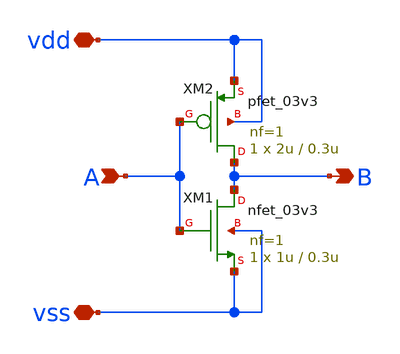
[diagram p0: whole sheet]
** sch_path: General/ADC/switching/inv4switch.sch
**.subckt inv4switch A B vdd vss
*.ipin A
*.opin B
*.iopin vdd
*.iopin vss
XM1 B A vss vss nfet_03v3 L=0.3u W=1u nf=1 ad='int((nf+1)/2) * W/nf * 0.18u' as='int((nf+2)/2) * W/nf * 0.18u'
+ pd='2*int((nf+1)/2) * (W/nf + 0.18u)' ps='2*int((nf+2)/2) * (W/nf + 0.18u)' nrd='0.18u / W' nrs='0.18u / W'
+ sa=0 sb=0 sd=0 m=1
XM2 B A vdd vdd pfet_03v3 L=0.3u W=2u nf=1 ad='int((nf+1)/2) * W/nf * 0.18u' as='int((nf+2)/2) * W/nf * 0.18u'
+ pd='2*int((nf+1)/2) * (W/nf + 0.18u)' ps='2*int((nf+2)/2) * (W/nf + 0.18u)' nrd='0.18u / W' nrs='0.18u / W'
+ sa=0 sb=0 sd=0 m=1
**.ends
.end
